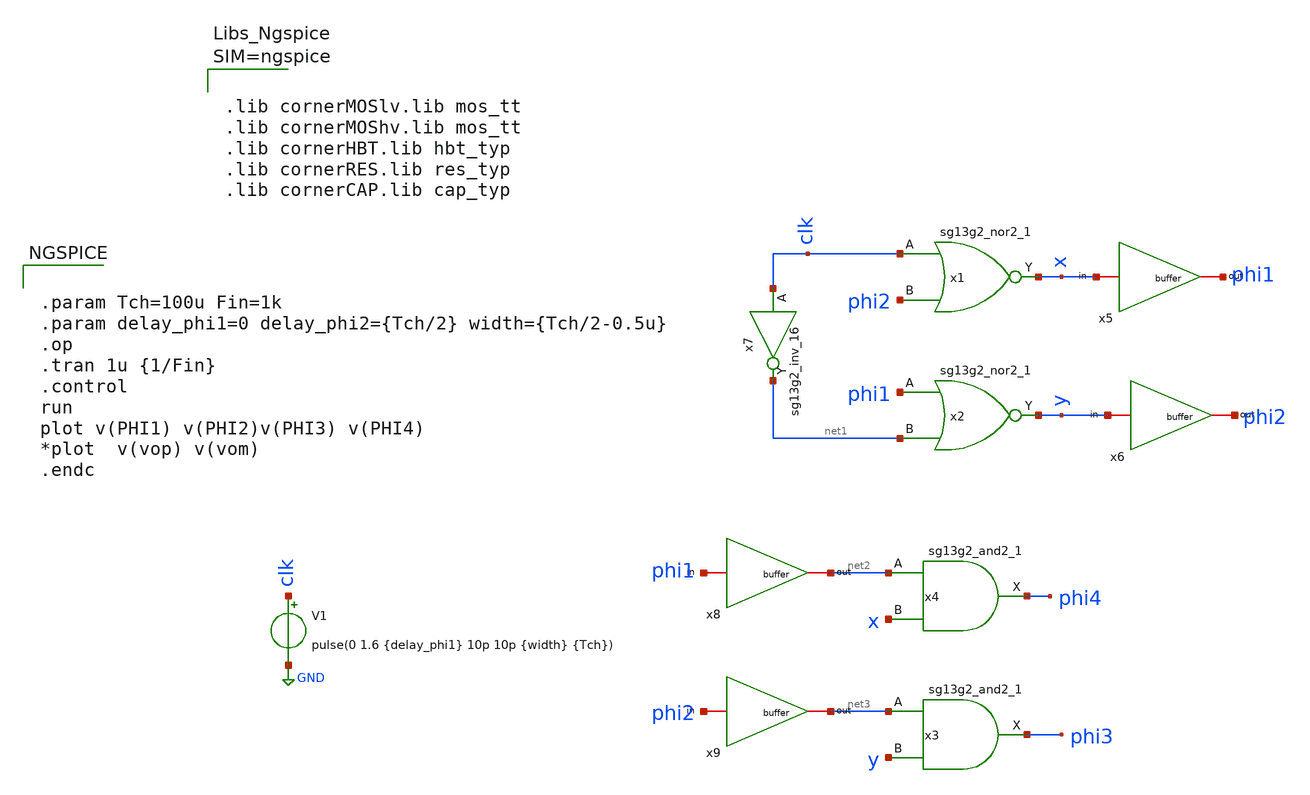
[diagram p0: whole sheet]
** sch_path: clock_gen_cycle/clock.sch
* IHP-GmbH/IHP-Open-PDK/ihp-sg13g2/libs.tech/xschem/sg13g2_stdcells/sg13g2_inv_16.sch:
* Copyright 2023 IHP PDK Authors
* Licensed under the Apache License, Version 2.0 (the "License");
**.subckt clock
x1 x clk phi2 VDD VSS sg13g2_nor2_1
x2 y phi1 net1 VDD VSS sg13g2_nor2_1
x4 phi4 net2 x VDD VSS sg13g2_and2_1
x3 phi3 net3 y VDD VSS sg13g2_and2_1
x5 x phi1 buffer
x6 y phi2 buffer
x7 net1 clk VDD VSS sg13g2_inv_16
x8 phi1 net2 buffer
x9 phi2 net3 buffer
V1 clk GND pulse(0 1.6 {delay_phi1} 10p 10p {width} {Tch})
**** begin user architecture code


.param Tch=100u Fin=1k
.param delay_phi1=0 delay_phi2={Tch/2} width={Tch/2-0.5u}
.op
.tran 1u {1/Fin}
.control
run
plot v(PHI1) v(PHI2)v(PHI3) v(PHI4)
*plot  v(vop) v(vom)
.endc





.lib cornerMOSlv.lib mos_tt
.lib cornerMOShv.lib mos_tt
.lib cornerHBT.lib hbt_typ
.lib cornerRES.lib res_typ
.lib cornerCAP.lib cap_typ



**** end user architecture code
**.ends

* expanding   symbol:  sg13g2_stdcells/sg13g2_nor2_1.sym # of pins=3
** sym_path: sg13g2_stdcells/sg13g2_nor2_1.sym
** sch_path: sg13g2_stdcells/sg13g2_nor2_1.sch
.subckt sg13g2_nor2_1 Y A B VDD VSS
*.opin Y
*.ipin B
*.ipin A
*.iopin VDD
*.iopin VSS
XM1 Y A VSS VSS sg13_lv_nmos w=740.00n l=130.00n ng=1 m=1 mm_ok=1
XM2 Y B VSS VSS sg13_lv_nmos w=740.00n l=130.00n ng=1 m=1 mm_ok=1
XM3 net1 A VDD VDD sg13_lv_pmos w=1.12u l=130.00n ng=1 m=1 mm_ok=1
XM4 Y B net1 VDD sg13_lv_pmos w=1.12u l=130.00n ng=1 m=1 mm_ok=1
.ends


* expanding   symbol:  sg13g2_stdcells/sg13g2_and2_1.sym # of pins=3
** sym_path: sg13g2_stdcells/sg13g2_and2_1.sym
** sch_path: sg13g2_stdcells/sg13g2_and2_1.sch
.subckt sg13g2_and2_1 X A B VDD VSS
*.ipin A
*.ipin B
*.opin X
*.iopin VDD
*.iopin VSS
XM1 net1 A net2 VSS sg13_lv_nmos w=640.00n l=130.00n ng=1 m=1 mm_ok=1
XM2 net2 B VSS VSS sg13_lv_nmos w=640.00n l=130.00n ng=1 m=1 mm_ok=1
XM3 X net1 VSS VSS sg13_lv_nmos w=740.00n l=130.00n ng=1 m=1 mm_ok=1
XM4 net1 B VDD VDD sg13_lv_pmos w=840.00n l=130.00n ng=1 m=1 mm_ok=1
XM5 net1 A VDD VDD sg13_lv_pmos w=840.00n l=130.00n ng=1 m=1 mm_ok=1
XM6 X net1 VDD VDD sg13_lv_pmos w=1.12u l=130.00n ng=1 m=1 mm_ok=1
.ends


* expanding   symbol:  /home/designer/shared/uni_cass/final_Design_file/clock_gen_cycle/buffer.sym #
*+ of pins=2
** sym_path: clock_gen_cycle/buffer.sym
** sch_path: clock_gen_cycle/buffer.sch
.subckt buffer in out
*.iopin in
*.iopin out
x1 net1 in VDD VSS sg13g2_buf_16
x2 out net1 VDD VSS sg13g2_buf_16
.ends


* expanding   symbol:  sg13g2_stdcells/sg13g2_inv_16.sym # of pins=2
** sym_path: sg13g2_stdcells/sg13g2_inv_16.sym
** sch_path: sg13g2_stdcells/sg13g2_inv_16.sch
.subckt sg13g2_inv_16 Y A VDD VSS
*.opin Y
*.iopin VSS
*.ipin A
*.iopin VDD
XM1 Y A VSS VSS sg13_lv_nmos w=11.84u l=130.00n ng=16 m=1 mm_ok=1
XM2 Y A VDD VDD sg13_lv_pmos w=17.92u l=130.00n ng=16 m=1 mm_ok=1
.ends


* expanding   symbol:  sg13g2_stdcells/sg13g2_buf_16.sym # of pins=2
** sym_path: sg13g2_stdcells/sg13g2_buf_16.sym
** sch_path: sg13g2_stdcells/sg13g2_buf_16.sch
.subckt sg13g2_buf_16 X A VDD VSS
*.ipin A
*.opin X
*.iopin VDD
*.iopin VSS
XM1 net1 A VSS VSS sg13_lv_nmos w=4.44u l=130.00n ng=6 m=1 mm_ok=1
XM2 X net1 VSS VSS sg13_lv_nmos w=11.84u l=130.00n ng=16 m=1 mm_ok=1
XM3 net1 A VDD VDD sg13_lv_pmos w=6.72u l=130.00n ng=6 m=1 mm_ok=1
XM4 X net1 VDD VDD sg13_lv_pmos w=17.92u l=130.00n ng=16 m=1 mm_ok=1
.ends

.GLOBAL GND
.end
